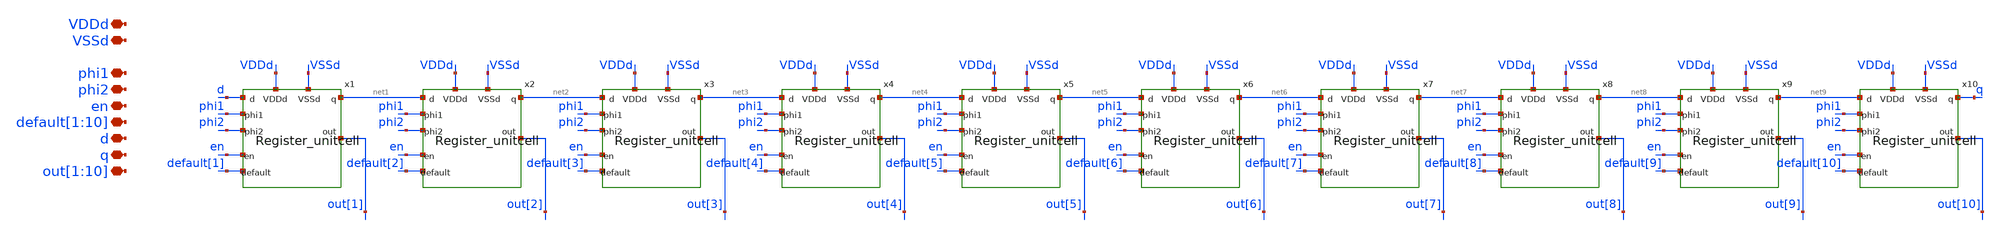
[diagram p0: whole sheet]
** sch_path: designs/libs/qw_core_analog/SRegister_10/SRegister_10.sch
**.subckt SRegister_10 VDDd VSSd phi1 phi2 en
*+ default[1],default[2],default[3],default[4],default[5],default[6],default[7],default[8],default[9],default[10] d q out[1],out[2],out[3],out[4],out[5],out[6],out[7],out[8],out[9],out[10]
*.iopin VDDd
*.iopin VSSd
*.iopin phi1
*.iopin phi2
*.iopin en
*.iopin
*+ default[1],default[2],default[3],default[4],default[5],default[6],default[7],default[8],default[9],default[10]
*.iopin d
*.iopin q
*.iopin out[1],out[2],out[3],out[4],out[5],out[6],out[7],out[8],out[9],out[10]
x1 net1 d phi1 phi2 VDDd VSSd out[1] en default[1] Register_unitcell
x2 net2 net1 phi1 phi2 VDDd VSSd out[2] en default[2] Register_unitcell
x3 net3 net2 phi1 phi2 VDDd VSSd out[3] en default[3] Register_unitcell
x4 net4 net3 phi1 phi2 VDDd VSSd out[4] en default[4] Register_unitcell
x5 net5 net4 phi1 phi2 VDDd VSSd out[5] en default[5] Register_unitcell
x6 net6 net5 phi1 phi2 VDDd VSSd out[6] en default[6] Register_unitcell
x7 net7 net6 phi1 phi2 VDDd VSSd out[7] en default[7] Register_unitcell
x8 net8 net7 phi1 phi2 VDDd VSSd out[8] en default[8] Register_unitcell
x9 net9 net8 phi1 phi2 VDDd VSSd out[9] en default[9] Register_unitcell
x10 q net9 phi1 phi2 VDDd VSSd out[10] en default[10] Register_unitcell
**.ends

* expanding   symbol:  Register_unitcell/Register_unitcell.sym # of pins=9
** sym_path: designs/libs/qw_core_analog/Register_unitcell/Register_unitcell.sym
** sch_path: designs/libs/qw_core_analog/Register_unitcell/Register_unitcell.sch
.subckt Register_unitcell q d phi1 phi2 VDDd VSSd out en default
*.iopin phi1
*.iopin phi2
*.iopin d
*.iopin q
*.iopin en
*.iopin default
*.iopin out
*.iopin VDDd
*.iopin VSSd
x1 d q phi1 phi2 DFF_2phase_1
x3 q en VSSd VDDd VSSd VDDd orb1 gf180mcu_fd_sc_mcu9t5v0__nand2_1
x4 en VSSd VDDd VSSd VDDd enbar gf180mcu_fd_sc_mcu9t5v0__inv_1
x5 or1 or2 VSSd VDDd VSSd VDDd net1 gf180mcu_fd_sc_mcu9t5v0__nor2_1
x6 orb1 VSSd VDDd VSSd VDDd or1 gf180mcu_fd_sc_mcu9t5v0__inv_1
x7 enbar default VSSd VDDd VSSd VDDd orb2 gf180mcu_fd_sc_mcu9t5v0__nand2_1
x8 orb2 VSSd VDDd VSSd VDDd or2 gf180mcu_fd_sc_mcu9t5v0__inv_1
x9 net1 VSSd VDDd VSSd VDDd out gf180mcu_fd_sc_mcu9t5v0__inv_1
* noconn VDDd
* noconn VSSd
.ends


* expanding   symbol:  switch_matrix_gf180mcu_9t5v0-main/DFF_2phase_1/DFF_2phase_1.sym # of pins=4
** sym_path: designs/switch_matrix_gf180mcu_9t5v0-main/designs/libs/core_swmatrix/DFF_2phase_1.sym
** sch_path: designs/switch_matrix_gf180mcu_9t5v0-main/designs/libs/core_swmatrix/DFF_2phase_1.sch
.subckt DFF_2phase_1 D Q PHI_1 PHI_2
*.ipin D
*.ipin PHI_1
*.ipin PHI_2
*.opin Q
xmain D PHI_1 out_m VDDd VDDd VSSd VSSd gf180mcu_fd_sc_mcu9t5v0__latq_1
xsecondary out_m PHI_2 Q VDDd VDDd VSSd VSSd gf180mcu_fd_sc_mcu9t5v0__latq_1
.ends

.end
